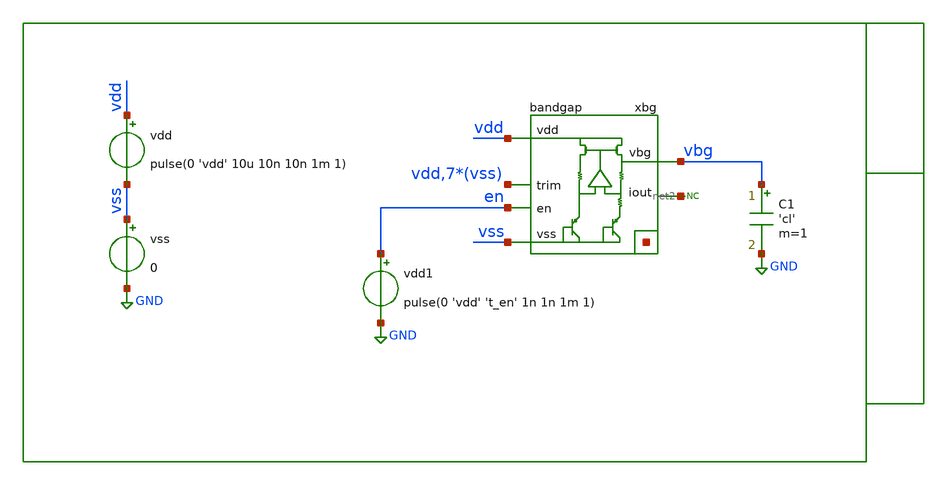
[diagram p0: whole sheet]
** sch_path: xschem/tb/bandgap_cm/bandgap/tr_bandgap_temperature.sch
**.subckt tr_bandgap_temperature
xbg vdd vbg vss net1[7] net1[6] net1[5] net1[4] net1[3] net1[2] net1[1] net1[0] vdd vss vss vss vss
+ vss vss vss net2 en bandgap
vss vss GND 0
C1 vbg GND 'cl' m=1
vdd vdd vss pulse(0 'vdd' 10u 10n 10n 1m 1)
* noconn #net2
vdd1 en GND pulse(0 'vdd' 't_en' 1n 1n 1m 1)
**** begin user architecture code

* Control

.options reltol = 1e-6

.param vdd  = 3.3
.param cl   = 100e-15
.param t_en = 20u

.temp 27


.control
save all
tran 1u 200u

meas tran vbg_avg avg v(vbg) from=150e-6 to=199e-6

print vbg_avg

set wr_singlescale
set wr_vecnames
wrdata data.csv vbg

.endc
.end


 * Model Corners

.include $::CORNERS/ngspice/tt.spice
*.include $::CORNERS/ngspice/ff.spice
*.include $::CORNERS/ngspice/ss.spice
*.include $::CORNERS/ngspice/sf.spice
*.include $::CORNERS/ngspice/fs.spice

**** end user architecture code
**.ends
.GLOBAL GND
.end
